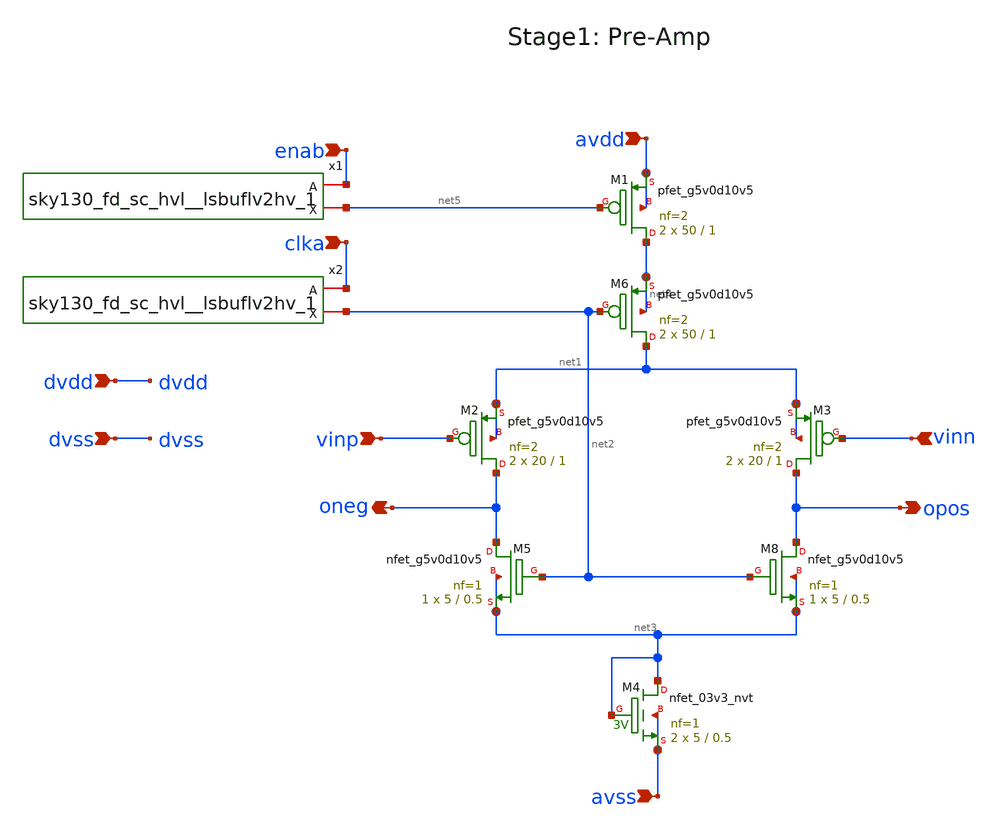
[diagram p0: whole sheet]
** sch_path: xschem/Stage1.sch
**.subckt Stage1 avdd vinp vinn opos oneg clka enab dvdd avss dvss
*.ipin avdd
*.ipin vinp
*.ipin vinn
*.opin opos
*.opin oneg
*.ipin clka
*.ipin enab
*.ipin dvdd
*.ipin avss
*.ipin dvss
XM1 net4 net5 avdd avdd sky130_fd_pr__pfet_g5v0d10v5 L=1 W=50 nf=2 ad='int((nf+1)/2) * W/nf * 0.29' as='int((nf+2)/2) * W/nf * 0.29'
+ pd='2*int((nf+1)/2) * (W/nf + 0.29)' ps='2*int((nf+2)/2) * (W/nf + 0.29)' nrd='0.29 / W' nrs='0.29 / W'
+ sa=0 sb=0 sd=0 mult=2 m=2
x2 clka dvdd dvss dvss avdd avdd net2 sky130_fd_sc_hvl__lsbuflv2hv_1
XM6 net1 net2 net4 net4 sky130_fd_pr__pfet_g5v0d10v5 L=1 W=50 nf=2 ad='int((nf+1)/2) * W/nf * 0.29' as='int((nf+2)/2) * W/nf * 0.29'
+ pd='2*int((nf+1)/2) * (W/nf + 0.29)' ps='2*int((nf+2)/2) * (W/nf + 0.29)' nrd='0.29 / W' nrs='0.29 / W'
+ sa=0 sb=0 sd=0 mult=2 m=2
XM2 oneg vinp net1 net1 sky130_fd_pr__pfet_g5v0d10v5 L=1 W=20 nf=2 ad='int((nf+1)/2) * W/nf * 0.29' as='int((nf+2)/2) * W/nf * 0.29'
+ pd='2*int((nf+1)/2) * (W/nf + 0.29)' ps='2*int((nf+2)/2) * (W/nf + 0.29)' nrd='0.29 / W' nrs='0.29 / W'
+ sa=0 sb=0 sd=0 mult=2 m=2
XM3 opos vinn net1 net1 sky130_fd_pr__pfet_g5v0d10v5 L=1 W=20 nf=2 ad='int((nf+1)/2) * W/nf * 0.29' as='int((nf+2)/2) * W/nf * 0.29'
+ pd='2*int((nf+1)/2) * (W/nf + 0.29)' ps='2*int((nf+2)/2) * (W/nf + 0.29)' nrd='0.29 / W' nrs='0.29 / W'
+ sa=0 sb=0 sd=0 mult=2 m=2
XM4 net3 net3 avss avss sky130_fd_pr__nfet_03v3_nvt L=0.5 W=5 nf=1 ad='int((nf+1)/2) * W/nf * 0.29' as='int((nf+2)/2) * W/nf * 0.29'
+ pd='2*int((nf+1)/2) * (W/nf + 0.29)' ps='2*int((nf+2)/2) * (W/nf + 0.29)' nrd='0.29 / W' nrs='0.29 / W'
+ sa=0 sb=0 sd=0 mult=2 m=2
XM8 opos net2 net3 net3 sky130_fd_pr__nfet_g5v0d10v5 L=0.5 W=5 nf=1 ad='int((nf+1)/2) * W/nf * 0.29'
+ as='int((nf+2)/2) * W/nf * 0.29' pd='2*int((nf+1)/2) * (W/nf + 0.29)' ps='2*int((nf+2)/2) * (W/nf + 0.29)'
+ nrd='0.29 / W' nrs='0.29 / W' sa=0 sb=0 sd=0 mult=1 m=1
XM5 oneg net2 net3 net3 sky130_fd_pr__nfet_g5v0d10v5 L=0.5 W=5 nf=1 ad='int((nf+1)/2) * W/nf * 0.29'
+ as='int((nf+2)/2) * W/nf * 0.29' pd='2*int((nf+1)/2) * (W/nf + 0.29)' ps='2*int((nf+2)/2) * (W/nf + 0.29)'
+ nrd='0.29 / W' nrs='0.29 / W' sa=0 sb=0 sd=0 mult=1 m=1
x1 enab dvdd dvss dvss avdd avdd net5 sky130_fd_sc_hvl__lsbuflv2hv_1
**.ends
.end
